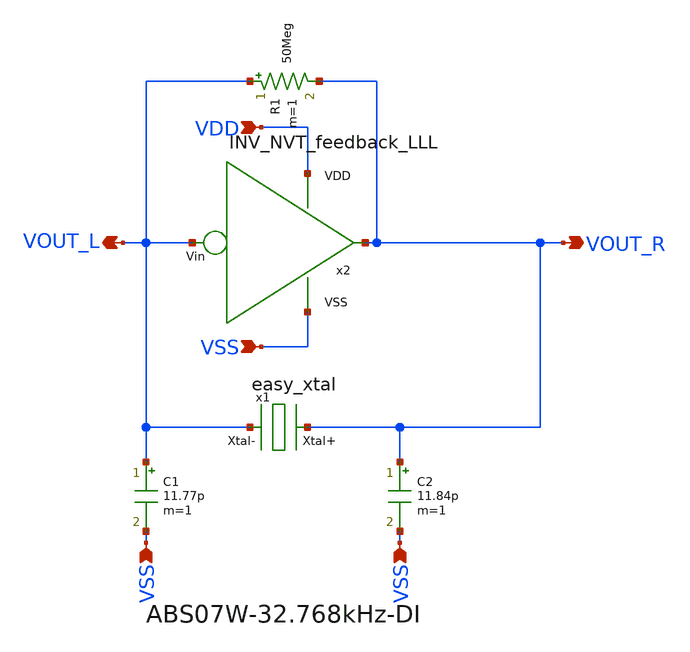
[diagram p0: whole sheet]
** sch_path: design/THESIS_EXP_RO_INVERTER_SKY130A/xtal_osc_NVT_LLL.sch
**.subckt xtal_osc_NVT_LLL VSS VSS VOUT_R VOUT_L VDD VSS
*.ipin VSS
*.ipin VSS
*.opin VOUT_R
*.opin VOUT_L
*.ipin VDD
*.ipin VSS
C1 VOUT_L VSS 11.77p m=1
C2 VOUT_R VSS 11.84p m=1
R1 VOUT_L VOUT_R 50Meg m=1
x2 VOUT_R VDD VSS VOUT_L INV_NVT_feedback_LLL
x1 VOUT_R VOUT_L easy_xtal
**.ends

* expanding   symbol:  THESIS_EXP_RO_INVERTER_SKY130A/INV_NVT_feedback_LLL.sym # of pins=4
** sym_path: design/THESIS_EXP_RO_INVERTER_SKY130A/INV_NVT_feedback_LLL.sym
** sch_path: design/THESIS_EXP_RO_INVERTER_SKY130A/INV_NVT_feedback_LLL.sch
.subckt INV_NVT_feedback_LLL Vout VDD VSS Vin
*.ipin VSS
*.ipin Vin
*.opin Vout
*.ipin VDD
XM1 Vout Vin VDD VDD sky130_fd_pr__pfet_01v8_lvt L=0.35 W=7 nf=1 ad='int((nf+1)/2) * W/nf * 0.29' as='int((nf+2)/2) * W/nf * 0.29'
+ pd='2*int((nf+1)/2) * (W/nf + 0.29)' ps='2*int((nf+2)/2) * (W/nf + 0.29)' nrd='0.29 / W' nrs='0.29 / W'
+ sa=0 sb=0 sd=0 mult=m_alpha m=m_alpha
XM2 net2 Vin vn VSS sky130_fd_pr__nfet_03v3_nvt L=0.8 W=0.42 nf=1 ad='int((nf+1)/2) * W/nf * 0.29' as='int((nf+2)/2) * W/nf * 0.29'
+ pd='2*int((nf+1)/2) * (W/nf + 0.29)' ps='2*int((nf+2)/2) * (W/nf + 0.29)' nrd='0.29 / W' nrs='0.29 / W'
+ sa=0 sb=0 sd=0 mult=m_beta m=m_beta
XM3 net1 Vin VSS VSS sky130_fd_pr__nfet_03v3_nvt L=0.8 W=0.42 nf=1 ad='int((nf+1)/2) * W/nf * 0.29' as='int((nf+2)/2) * W/nf * 0.29'
+ pd='2*int((nf+1)/2) * (W/nf + 0.29)' ps='2*int((nf+2)/2) * (W/nf + 0.29)' nrd='0.29 / W' nrs='0.29 / W'
+ sa=0 sb=0 sd=0 mult=m_I0 m=m_I0
XM4 VDD Vout net3 VSS sky130_fd_pr__nfet_03v3_nvt L=0.8 W=0.42 nf=1 ad='int((nf+1)/2) * W/nf * 0.29'
+ as='int((nf+2)/2) * W/nf * 0.29' pd='2*int((nf+1)/2) * (W/nf + 0.29)' ps='2*int((nf+2)/2) * (W/nf + 0.29)'
+ nrd='0.29 / W' nrs='0.29 / W' sa=0 sb=0 sd=0 mult=m_gamma m=m_gamma
XM5 Vout Vin net2 VSS sky130_fd_pr__nfet_03v3_nvt L=0.8 W=0.42 nf=1 ad='int((nf+1)/2) * W/nf * 0.29'
+ as='int((nf+2)/2) * W/nf * 0.29' pd='2*int((nf+1)/2) * (W/nf + 0.29)' ps='2*int((nf+2)/2) * (W/nf + 0.29)'
+ nrd='0.29 / W' nrs='0.29 / W' sa=0 sb=0 sd=0 mult=m_beta m=m_beta
XM6 vn Vin net1 VSS sky130_fd_pr__nfet_03v3_nvt L=0.8 W=0.42 nf=1 ad='int((nf+1)/2) * W/nf * 0.29' as='int((nf+2)/2) * W/nf * 0.29'
+ pd='2*int((nf+1)/2) * (W/nf + 0.29)' ps='2*int((nf+2)/2) * (W/nf + 0.29)' nrd='0.29 / W' nrs='0.29 / W'
+ sa=0 sb=0 sd=0 mult=m_I0 m=m_I0
XM7 net3 Vout vn VSS sky130_fd_pr__nfet_03v3_nvt L=0.8 W=0.42 nf=1 ad='int((nf+1)/2) * W/nf * 0.29' as='int((nf+2)/2) * W/nf * 0.29'
+ pd='2*int((nf+1)/2) * (W/nf + 0.29)' ps='2*int((nf+2)/2) * (W/nf + 0.29)' nrd='0.29 / W' nrs='0.29 / W'
+ sa=0 sb=0 sd=0 mult=m_gamma m=m_gamma
.ends


* expanding   symbol:  THESIS_EXP_RO_INVERTER_SKY130A/easy_xtal.sym # of pins=2
** sym_path: design/THESIS_EXP_RO_INVERTER_SKY130A/easy_xtal.sym
** sch_path: design/THESIS_EXP_RO_INVERTER_SKY130A/easy_xtal.sch
.subckt easy_xtal Xtal+ Xtal-
*.iopin Xtal+
*.iopin Xtal-
R1 Xtal+ net1 30k m=1
C1 net1 net2 7.4f m=1
L1 net2 Xtal- 3187 m=1
C2 Xtal+ Xtal- 1p m=1
.ends

.end
